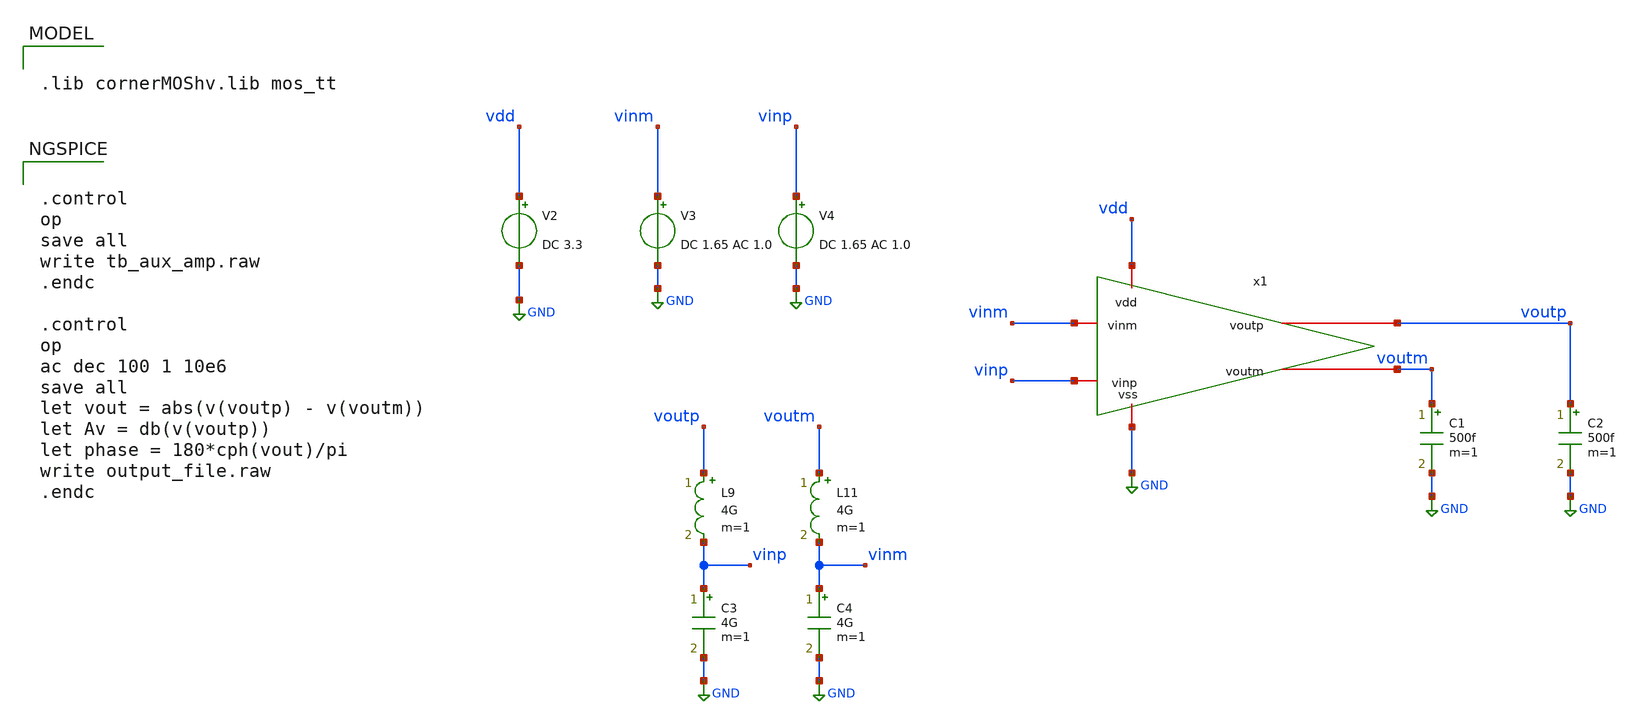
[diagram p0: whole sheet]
** sch_path: testbench/aux_amp_tb.sch
**.subckt aux_amp_tb
x1 vdd vinm vinp voutp voutm GND aux_amp
C1 voutm GND 500f m=1
C2 voutp GND 500f m=1
V2 vdd GND DC 3.3
V3 vinm GND DC 1.65 AC 1.0
V4 vinp GND DC 1.65 AC 1.0
L9 voutp vinp 4G m=1
C3 vinp GND 4G m=1
L11 voutm vinm 4G m=1
C4 vinm GND 4G m=1
**** begin user architecture code

.lib cornerMOShv.lib mos_tt



.control
op
save all
write tb_aux_amp.raw
.endc

.control
op
ac dec 100 1 10e6
save all
let vout = abs(v(voutp) - v(voutm))
let Av = db(v(voutp))
let phase = 180*cph(vout)/pi
write output_file.raw
.endc


**** end user architecture code
**.ends

* expanding   symbol:  /home/andreasp/diy-ic/schematic/aux_amp.sym # of pins=6
** sym_path: schematic/aux_amp.sym
** sch_path: schematic/aux_amp.sch
.subckt aux_amp vdd vinm vinp voutp voutm vss
*.iopin vss
*.iopin voutm
*.iopin vinp
*.iopin vdd
*.iopin voutp
*.iopin vinm
XM2 net3 vinp net1 net1 sg13_hv_nmos w=0.3u l=0.45u ng=1 m=1 mm_ok=1
XM3 net4 cm_bias net1 net1 sg13_hv_nmos w=0.3u l=0.45u ng=1 m=1 mm_ok=1
XM4 net1 nbias vss vss sg13_hv_nmos w=0.3u l=0.45u ng=1 m=1 mm_ok=1
XM6 net3 cm_bias net2 net2 sg13_hv_nmos w=0.3u l=0.45u ng=1 m=1 mm_ok=1
XM7 net4 vinm net2 net2 sg13_hv_nmos w=0.3u l=0.45u ng=1 m=1 mm_ok=1
XM8 net2 nbias vss vss sg13_hv_nmos w=0.3u l=0.45u ng=1 m=1 mm_ok=1
XM9 voutm nbias vss vss sg13_hv_nmos w=0.3u l=0.45u ng=1 m=1 mm_ok=1
XM11 voutp nbias vss vss sg13_hv_nmos w=0.3u l=0.45u ng=1 m=1 mm_ok=1
V2 pbias_top vss 1.65
V3 pbias vss 1.65
V4 cm_bias vss 1.65
V1 nbias vss 1.65
XM1 voutm pbias net3 net3 sg13_hv_pmos w=0.3u l=0.4u ng=1 m=1 mm_ok=1
XM5 net3 pbias_top vdd vdd sg13_hv_pmos w=0.3u l=0.4u ng=1 m=1 mm_ok=1
XM10 net4 pbias_top vdd vdd sg13_hv_pmos w=0.3u l=0.4u ng=1 m=1 mm_ok=1
XM12 voutp pbias net4 net4 sg13_hv_pmos w=0.3u l=0.4u ng=1 m=1 mm_ok=1
.ends

.GLOBAL GND
.end
